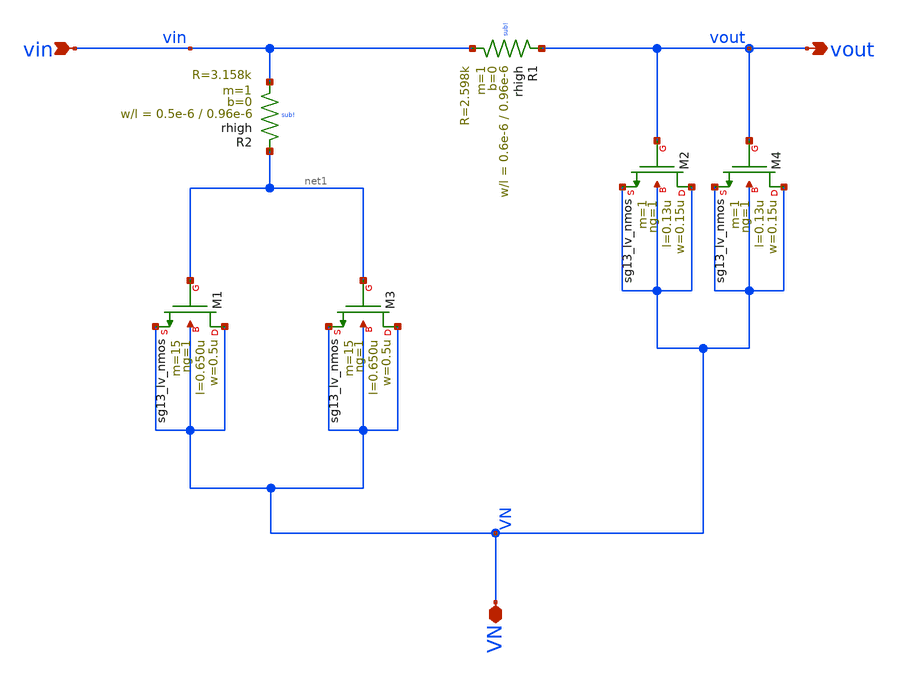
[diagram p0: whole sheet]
** sch_path: Combined Design/design_data/xschem/loop_filter.sch
**.subckt loop_filter VN vin vout
*.iopin VN
*.ipin vin
*.opin vout
XR1 vout vin sub! rhigh w=0.6e-6 l=0.96e-6 m=1 b=0 mm_ok=1
XM1 VN net1 VN VN sg13_lv_nmos w=0.5u l=0.650u ng=1 m=15 mm_ok=1
XM2 VN vout VN VN sg13_lv_nmos w=0.15u l=0.13u ng=1 m=1 mm_ok=1
XM3 VN net1 VN VN sg13_lv_nmos w=0.5u l=0.650u ng=1 m=15 mm_ok=1
XM4 VN vout VN VN sg13_lv_nmos w=0.15u l=0.13u ng=1 m=1 mm_ok=1
XR2 net1 vin sub! rhigh w=0.5e-6 l=0.96e-6 m=1 b=0 mm_ok=1
**.ends
.end
